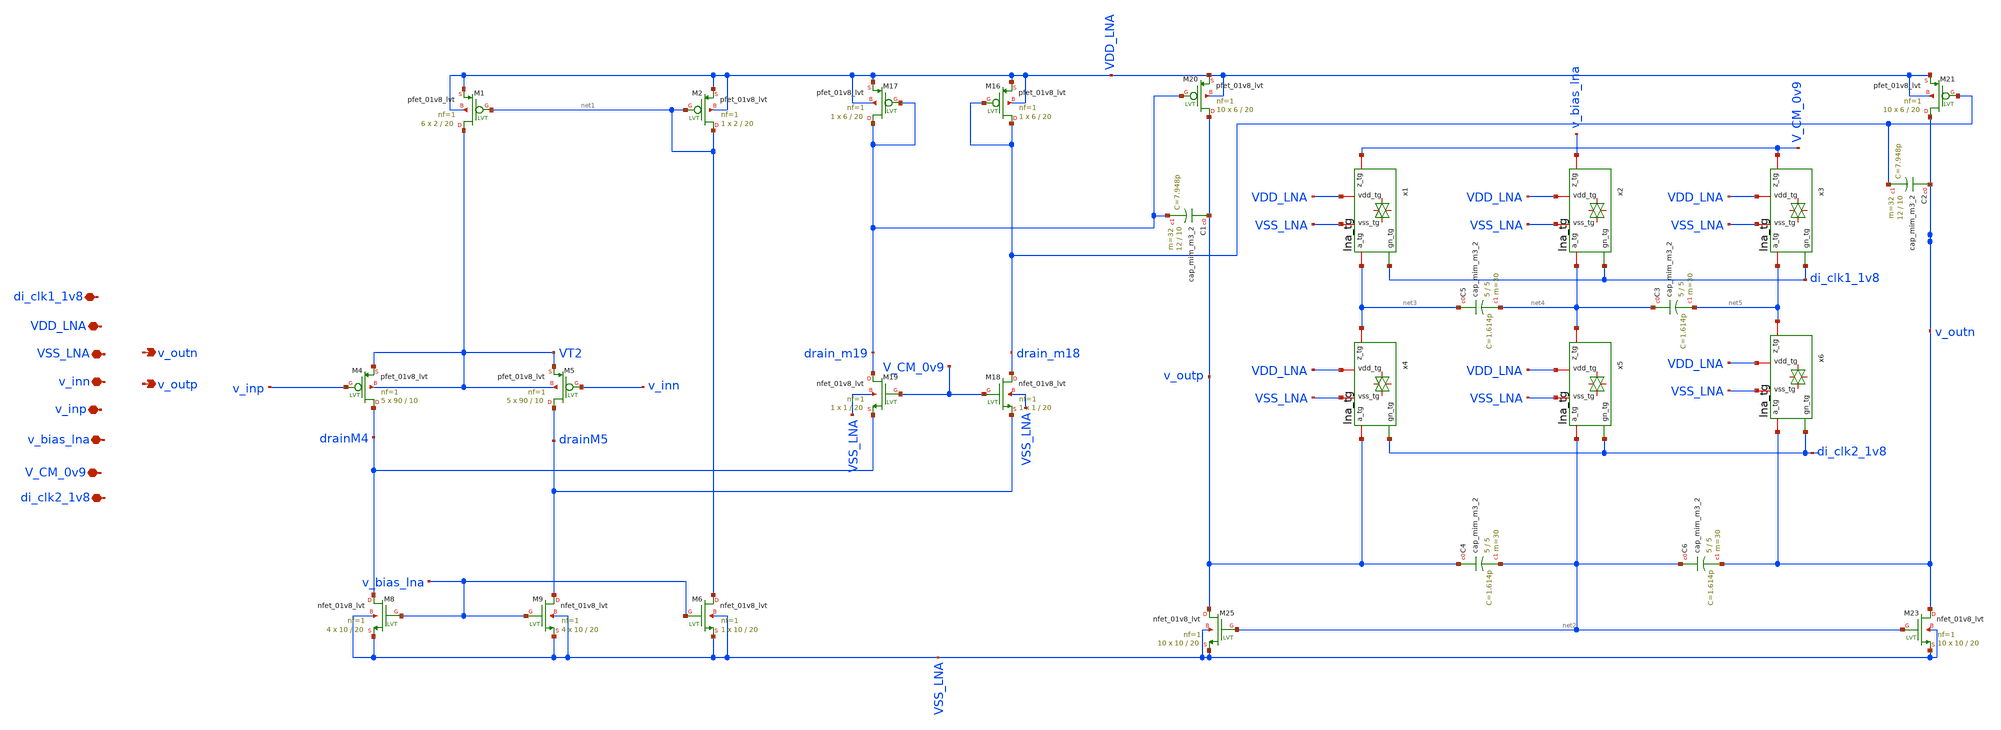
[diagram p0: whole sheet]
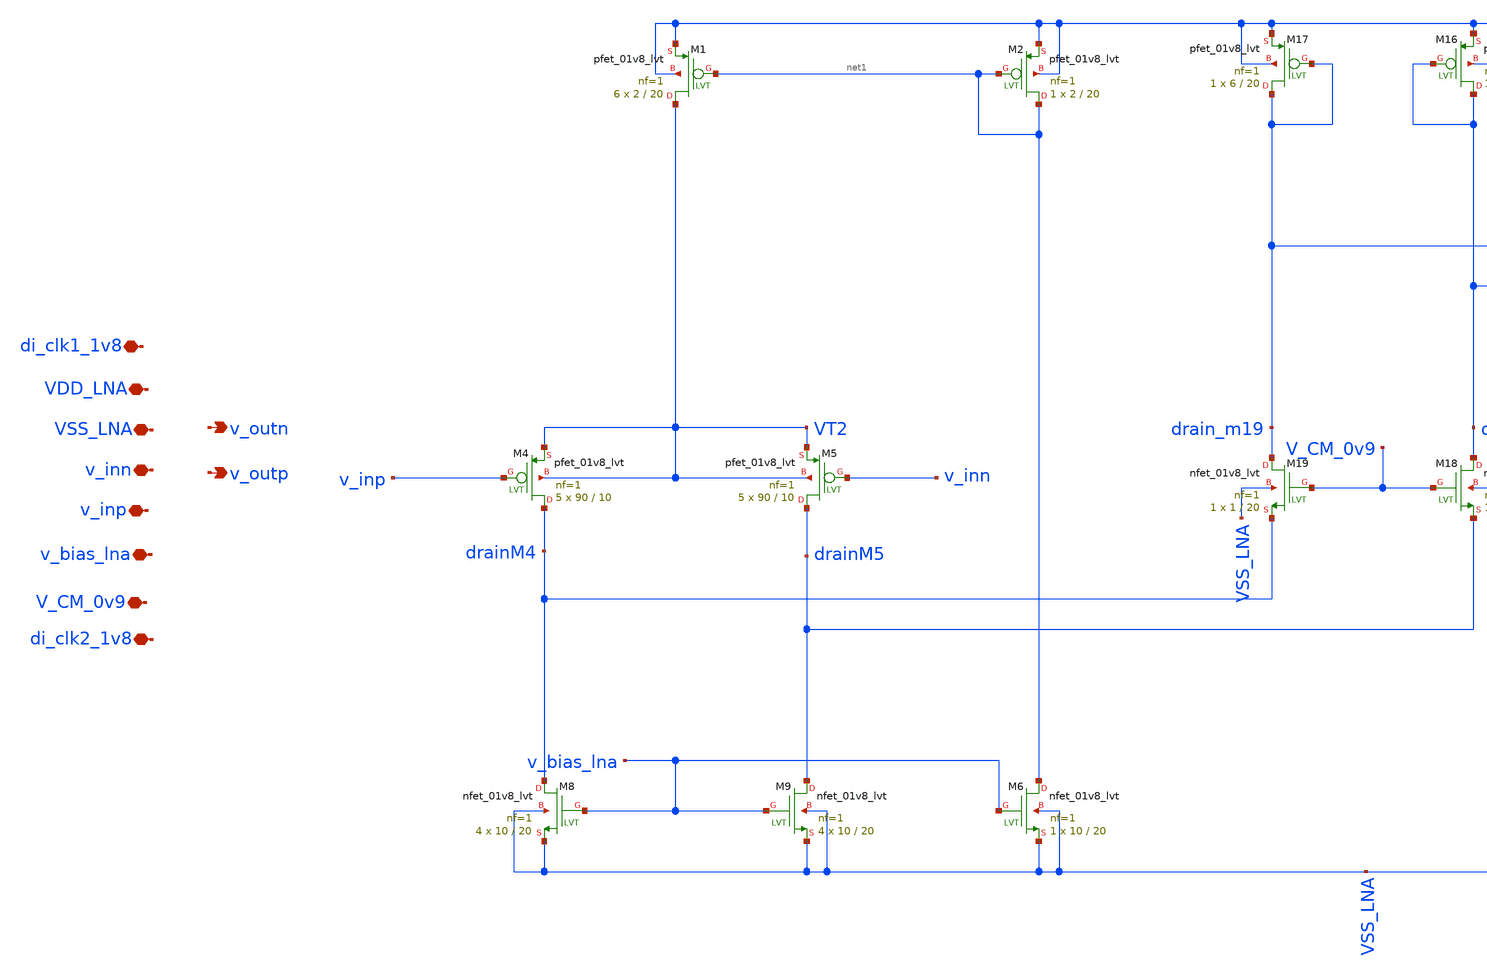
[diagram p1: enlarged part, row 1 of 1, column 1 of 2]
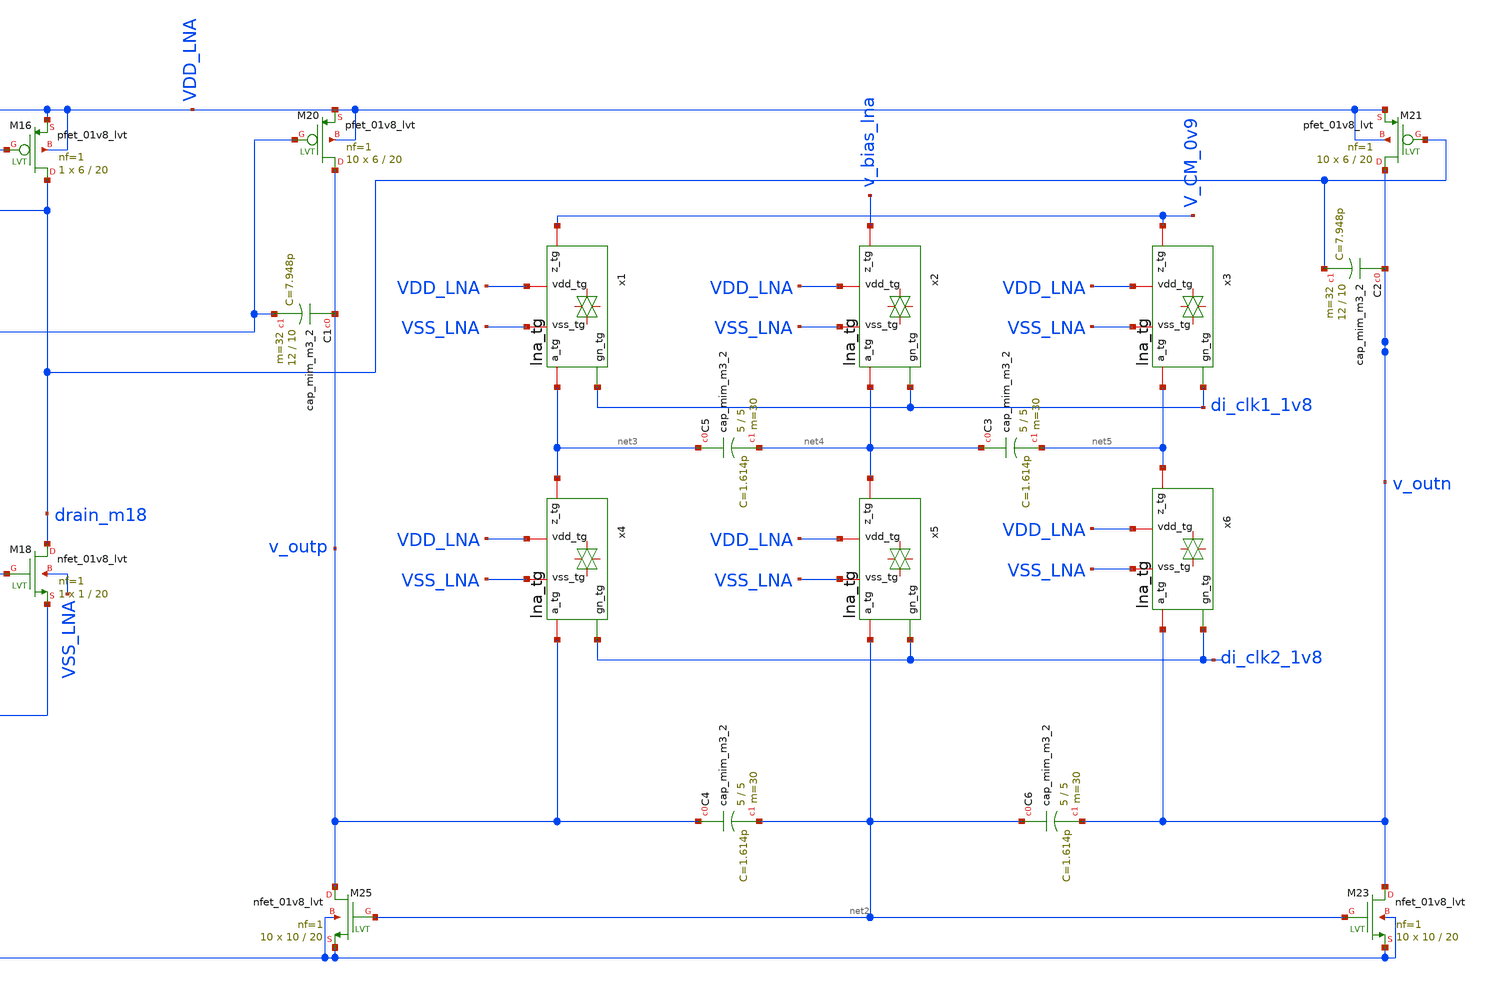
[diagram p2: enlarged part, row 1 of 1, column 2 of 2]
** sch_path: core.sch
**.subckt core v_inp v_inn VSS_LNA VDD_LNA V_CM_0v9 v_outp v_outn di_clk2_1v8 v_bias_lna di_clk1_1v8
*.iopin v_inp
*.iopin v_inn
*.iopin VSS_LNA
*.iopin VDD_LNA
*.iopin V_CM_0v9
*.opin v_outp
*.opin v_outn
*.iopin di_clk2_1v8
*.iopin v_bias_lna
*.iopin di_clk1_1v8
XM4 drainM4 v_inp VT2 VT2 sky130_fd_pr__pfet_01v8_lvt L=10 W=90 nf=1 ad='int((nf+1)/2) * W/nf * 0.29'
+ as='int((nf+2)/2) * W/nf * 0.29' pd='2*int((nf+1)/2) * (W/nf + 0.29)' ps='2*int((nf+2)/2) * (W/nf + 0.29)'
+ nrd='0.29 / W' nrs='0.29 / W' sa=0 sb=0 sd=0 mult=5 m=5
XM5 drainM5 v_inn VT2 VT2 sky130_fd_pr__pfet_01v8_lvt L=10 W=90 nf=1 ad='int((nf+1)/2) * W/nf * 0.29'
+ as='int((nf+2)/2) * W/nf * 0.29' pd='2*int((nf+1)/2) * (W/nf + 0.29)' ps='2*int((nf+2)/2) * (W/nf + 0.29)'
+ nrd='0.29 / W' nrs='0.29 / W' sa=0 sb=0 sd=0 mult=5 m=5
XM8 drainM4 v_bias_lna VSS_LNA VSS_LNA sky130_fd_pr__nfet_01v8_lvt L=20 W=10 nf=1 ad='int((nf+1)/2) * W/nf * 0.29'
+ as='int((nf+2)/2) * W/nf * 0.29' pd='2*int((nf+1)/2) * (W/nf + 0.29)' ps='2*int((nf+2)/2) * (W/nf + 0.29)'
+ nrd='0.29 / W' nrs='0.29 / W' sa=0 sb=0 sd=0 mult=4 m=4
XM9 drainM5 v_bias_lna VSS_LNA VSS_LNA sky130_fd_pr__nfet_01v8_lvt L=20 W=10 nf=1 ad='int((nf+1)/2) * W/nf * 0.29'
+ as='int((nf+2)/2) * W/nf * 0.29' pd='2*int((nf+1)/2) * (W/nf + 0.29)' ps='2*int((nf+2)/2) * (W/nf + 0.29)'
+ nrd='0.29 / W' nrs='0.29 / W' sa=0 sb=0 sd=0 mult=4 m=4
XM16 drain_m18 drain_m18 VDD_LNA VDD_LNA sky130_fd_pr__pfet_01v8_lvt L=20 W=6 nf=1 ad='int((nf+1)/2) * W/nf * 0.29'
+ as='int((nf+2)/2) * W/nf * 0.29' pd='2*int((nf+1)/2) * (W/nf + 0.29)' ps='2*int((nf+2)/2) * (W/nf + 0.29)'
+ nrd='0.29 / W' nrs='0.29 / W' sa=0 sb=0 sd=0 mult=1 m=1
XM17 drain_m19 drain_m19 VDD_LNA VDD_LNA sky130_fd_pr__pfet_01v8_lvt L=20 W=6 nf=1 ad='int((nf+1)/2) * W/nf * 0.29'
+ as='int((nf+2)/2) * W/nf * 0.29' pd='2*int((nf+1)/2) * (W/nf + 0.29)' ps='2*int((nf+2)/2) * (W/nf + 0.29)'
+ nrd='0.29 / W' nrs='0.29 / W' sa=0 sb=0 sd=0 mult=1 m=1
XM18 drain_m18 V_CM_0v9 drainM5 VSS_LNA sky130_fd_pr__nfet_01v8_lvt L=20 W=1 nf=1 ad='int((nf+1)/2) * W/nf * 0.29'
+ as='int((nf+2)/2) * W/nf * 0.29' pd='2*int((nf+1)/2) * (W/nf + 0.29)' ps='2*int((nf+2)/2) * (W/nf + 0.29)'
+ nrd='0.29 / W' nrs='0.29 / W' sa=0 sb=0 sd=0 mult=1 m=1
XM19 drain_m19 V_CM_0v9 drainM4 VSS_LNA sky130_fd_pr__nfet_01v8_lvt L=20 W=1 nf=1 ad='int((nf+1)/2) * W/nf * 0.29'
+ as='int((nf+2)/2) * W/nf * 0.29' pd='2*int((nf+1)/2) * (W/nf + 0.29)' ps='2*int((nf+2)/2) * (W/nf + 0.29)'
+ nrd='0.29 / W' nrs='0.29 / W' sa=0 sb=0 sd=0 mult=1 m=1
XM20 v_outp drain_m19 VDD_LNA VDD_LNA sky130_fd_pr__pfet_01v8_lvt L=20 W=6 nf=1 ad='int((nf+1)/2) * W/nf * 0.29'
+ as='int((nf+2)/2) * W/nf * 0.29' pd='2*int((nf+1)/2) * (W/nf + 0.29)' ps='2*int((nf+2)/2) * (W/nf + 0.29)'
+ nrd='0.29 / W' nrs='0.29 / W' sa=0 sb=0 sd=0 mult=10 m=10
XM21 v_outn drain_m18 VDD_LNA VDD_LNA sky130_fd_pr__pfet_01v8_lvt L=20 W=6 nf=1 ad='int((nf+1)/2) * W/nf * 0.29'
+ as='int((nf+2)/2) * W/nf * 0.29' pd='2*int((nf+1)/2) * (W/nf + 0.29)' ps='2*int((nf+2)/2) * (W/nf + 0.29)'
+ nrd='0.29 / W' nrs='0.29 / W' sa=0 sb=0 sd=0 mult=10 m=10
XM23 v_outn net2 VSS_LNA VSS_LNA sky130_fd_pr__nfet_01v8_lvt L=20 W=10 nf=1 ad='int((nf+1)/2) * W/nf * 0.29'
+ as='int((nf+2)/2) * W/nf * 0.29' pd='2*int((nf+1)/2) * (W/nf + 0.29)' ps='2*int((nf+2)/2) * (W/nf + 0.29)'
+ nrd='0.29 / W' nrs='0.29 / W' sa=0 sb=0 sd=0 mult=10 m=10
XM25 v_outp net2 VSS_LNA VSS_LNA sky130_fd_pr__nfet_01v8_lvt L=20 W=10 nf=1 ad='int((nf+1)/2) * W/nf * 0.29'
+ as='int((nf+2)/2) * W/nf * 0.29' pd='2*int((nf+1)/2) * (W/nf + 0.29)' ps='2*int((nf+2)/2) * (W/nf + 0.29)'
+ nrd='0.29 / W' nrs='0.29 / W' sa=0 sb=0 sd=0 mult=10 m=10
XM1 VT2 net1 VDD_LNA VDD_LNA sky130_fd_pr__pfet_01v8_lvt L=20 W=2 nf=1 ad='int((nf+1)/2) * W/nf * 0.29'
+ as='int((nf+2)/2) * W/nf * 0.29' pd='2*int((nf+1)/2) * (W/nf + 0.29)' ps='2*int((nf+2)/2) * (W/nf + 0.29)'
+ nrd='0.29 / W' nrs='0.29 / W' sa=0 sb=0 sd=0 mult=6 m=6
XM2 net1 net1 VDD_LNA VDD_LNA sky130_fd_pr__pfet_01v8_lvt L=20 W=2 nf=1 ad='int((nf+1)/2) * W/nf * 0.29'
+ as='int((nf+2)/2) * W/nf * 0.29' pd='2*int((nf+1)/2) * (W/nf + 0.29)' ps='2*int((nf+2)/2) * (W/nf + 0.29)'
+ nrd='0.29 / W' nrs='0.29 / W' sa=0 sb=0 sd=0 mult=1 m=1
XM6 net1 v_bias_lna VSS_LNA VSS_LNA sky130_fd_pr__nfet_01v8_lvt L=20 W=10 nf=1 ad='int((nf+1)/2) * W/nf * 0.29'
+ as='int((nf+2)/2) * W/nf * 0.29' pd='2*int((nf+1)/2) * (W/nf + 0.29)' ps='2*int((nf+2)/2) * (W/nf + 0.29)'
+ nrd='0.29 / W' nrs='0.29 / W' sa=0 sb=0 sd=0 mult=1 m=1
XC1 v_outp drain_m19 sky130_fd_pr__cap_mim_m3_2 W=12 L=10 MF=32 m=32
XC2 v_outn drain_m18 sky130_fd_pr__cap_mim_m3_2 W=12 L=10 MF=32 m=32
x1 VDD_LNA net3 V_CM_0v9 VSS_LNA di_clk1_1v8 lna_tg
x2 VDD_LNA net4 v_bias_lna VSS_LNA di_clk1_1v8 lna_tg
x3 VDD_LNA net5 V_CM_0v9 VSS_LNA di_clk1_1v8 lna_tg
x4 VDD_LNA v_outp net3 VSS_LNA di_clk2_1v8 lna_tg
x5 VDD_LNA net2 net4 VSS_LNA di_clk2_1v8 lna_tg
XC5 net3 net4 sky130_fd_pr__cap_mim_m3_2 W=5 L=5 MF=30 m=30
x6 VDD_LNA v_outn net5 VSS_LNA di_clk2_1v8 lna_tg
XC3 net4 net5 sky130_fd_pr__cap_mim_m3_2 W=5 L=5 MF=30 m=30
XC4 v_outp net2 sky130_fd_pr__cap_mim_m3_2 W=5 L=5 MF=30 m=30
XC6 net2 v_outn sky130_fd_pr__cap_mim_m3_2 W=5 L=5 MF=30 m=30
**.ends
.end
